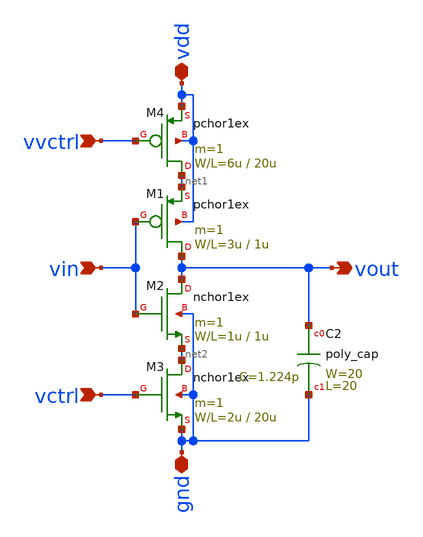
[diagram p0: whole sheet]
** sch_path: member_project/DCDC_DOWN/xschem/original_VCO/inverter.sch
**.subckt inverter vin vout vdd gnd vctrl vvctrl
*.ipin vin
*.opin vout
*.iopin vdd
*.iopin gnd
*.ipin vctrl
*.ipin vvctrl
M1 vout vin net1 vdd pchor1ex L=1u W=3u m=1
M2 vout vin net2 gnd nchor1ex L=1u W=1u m=1
M3 net2 vctrl gnd gnd nchor1ex L=20u W=2u m=1
M4 net1 vvctrl vdd vdd pchor1ex L=20u W=6u m=1
C2 vout gnd poly_cap W=20 L=20
**.ends
.end
